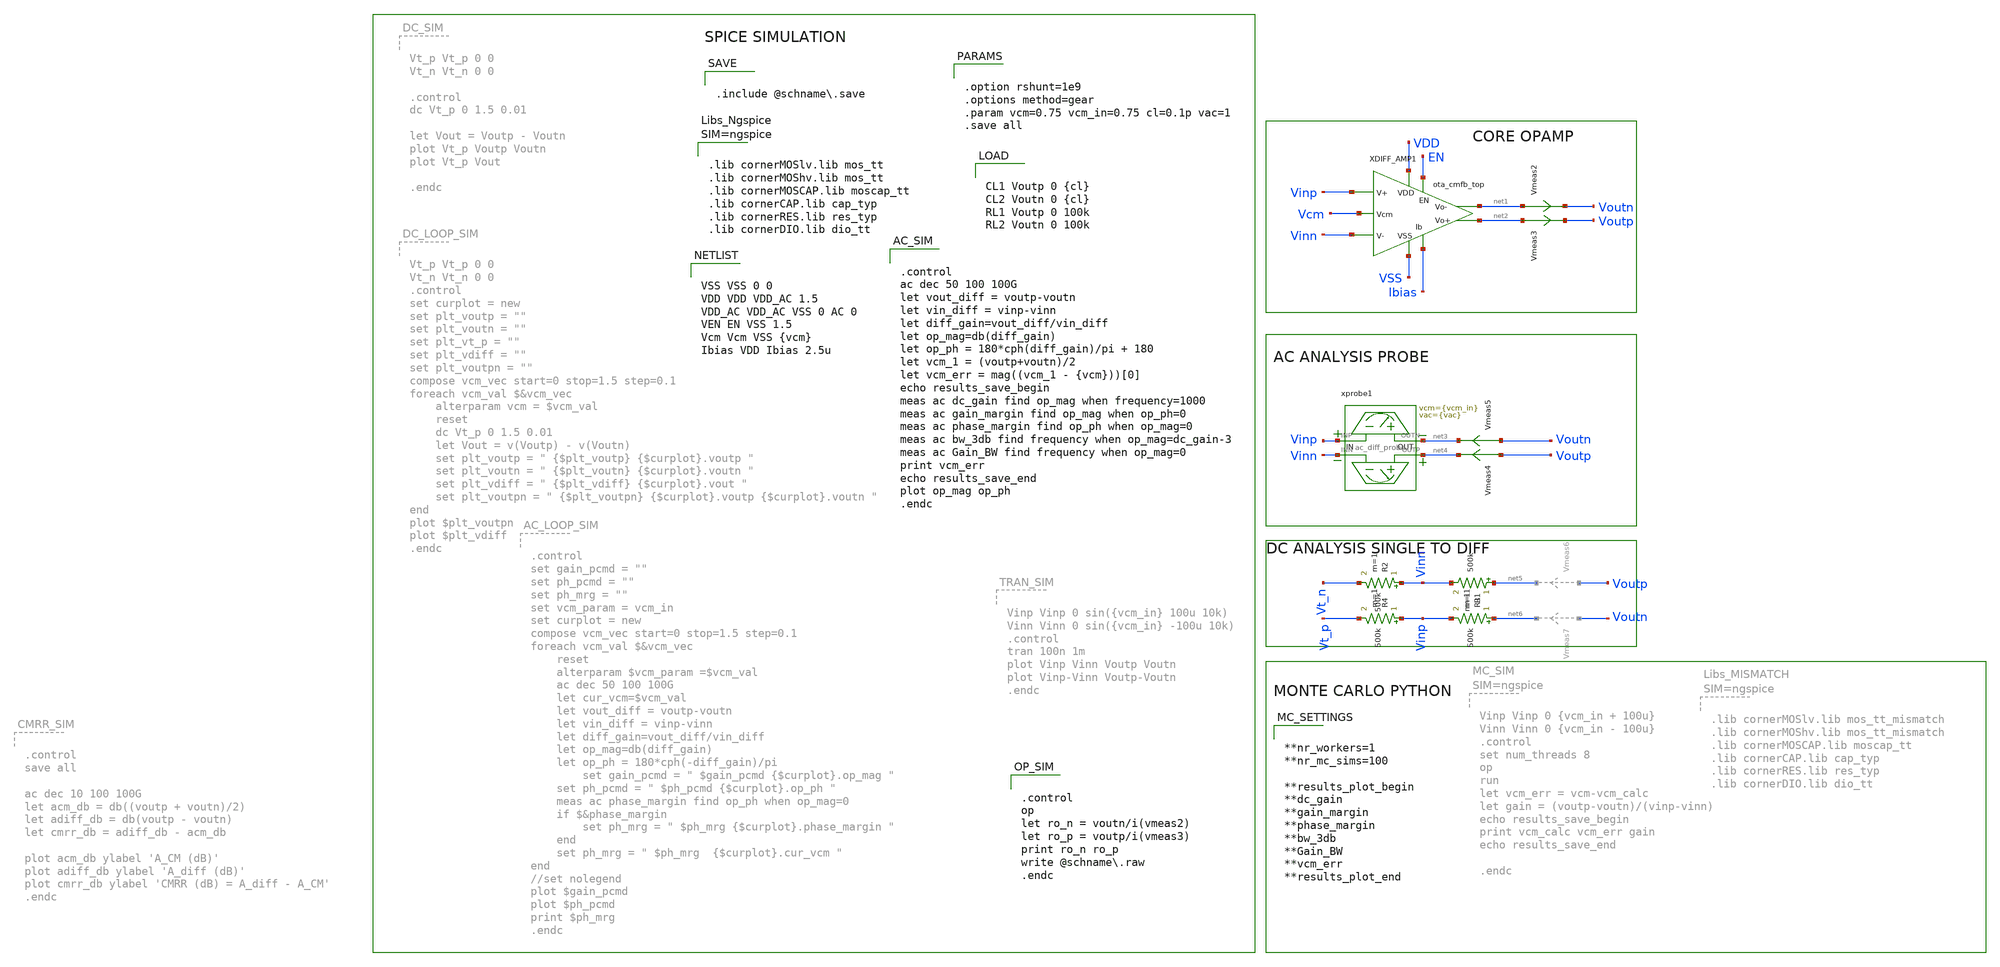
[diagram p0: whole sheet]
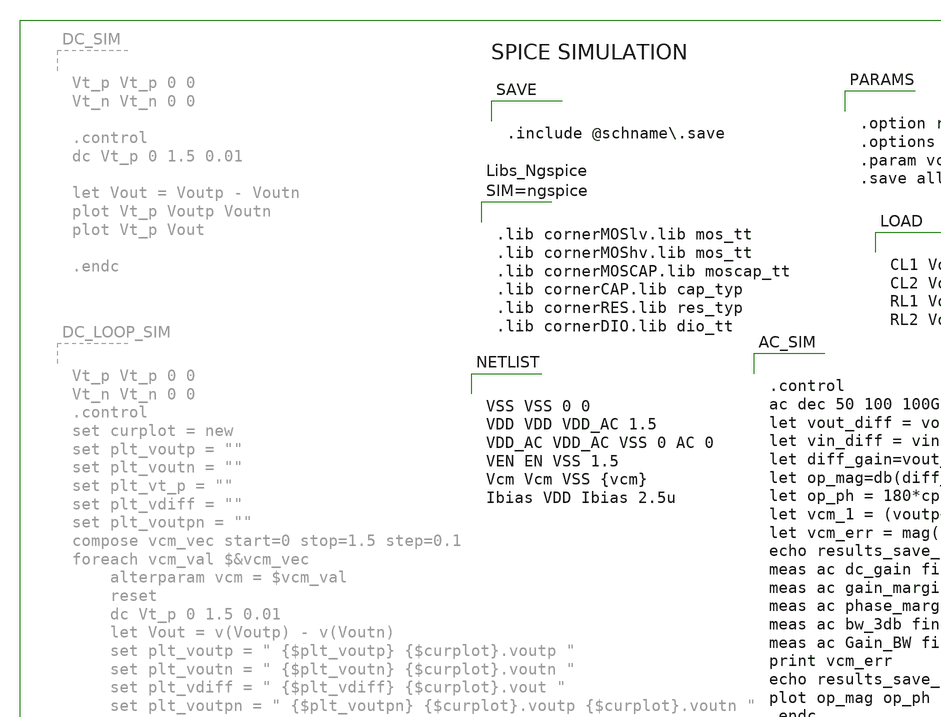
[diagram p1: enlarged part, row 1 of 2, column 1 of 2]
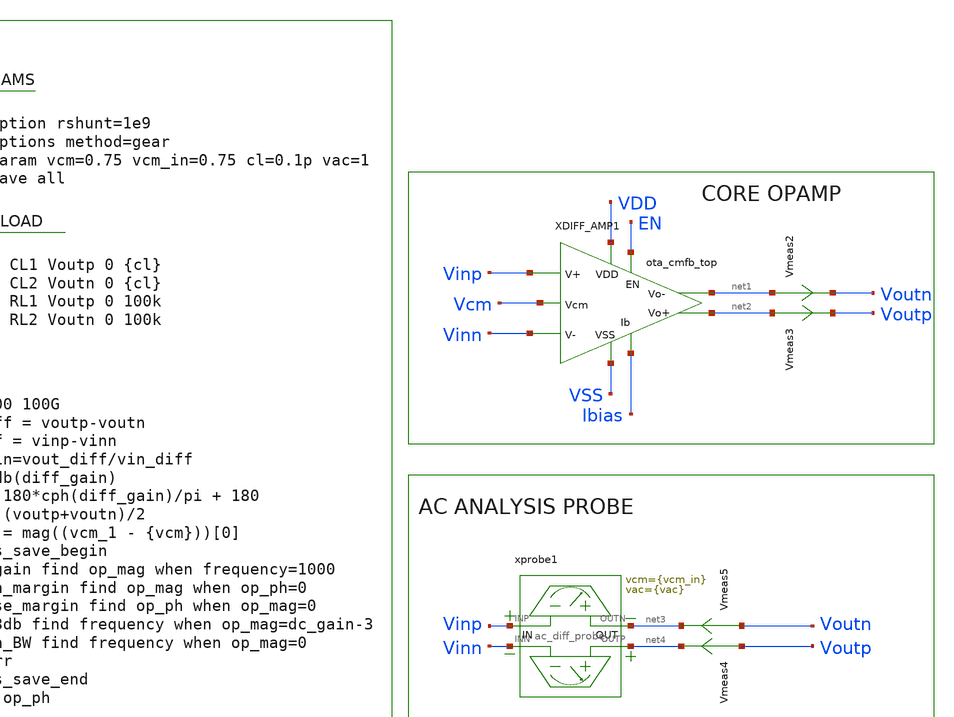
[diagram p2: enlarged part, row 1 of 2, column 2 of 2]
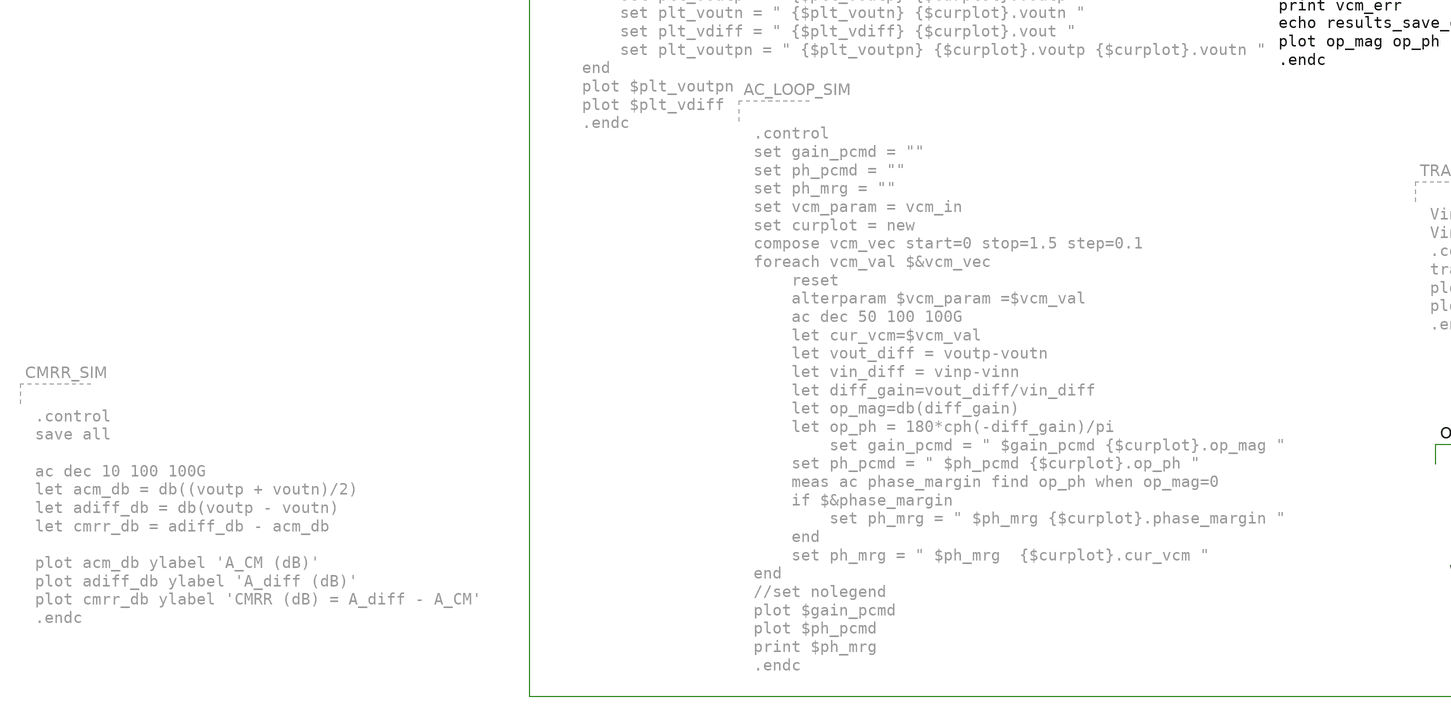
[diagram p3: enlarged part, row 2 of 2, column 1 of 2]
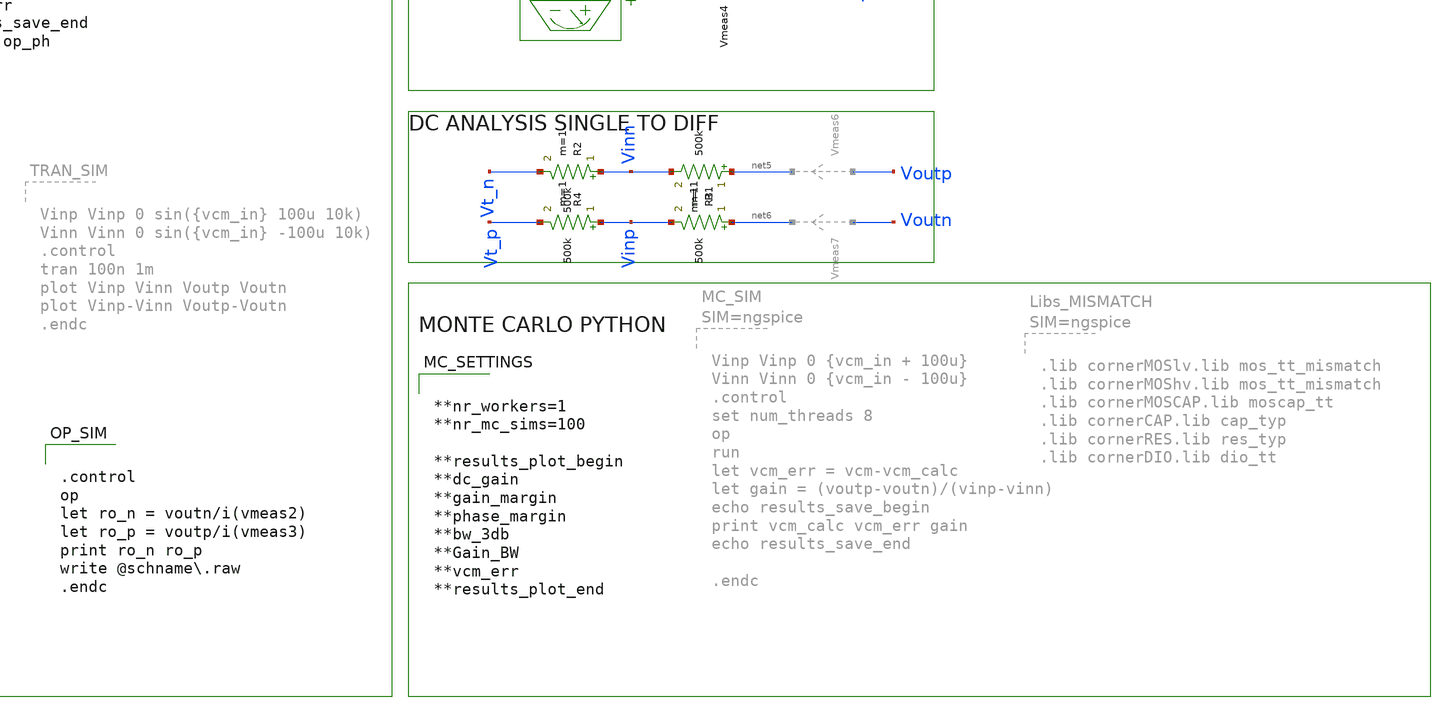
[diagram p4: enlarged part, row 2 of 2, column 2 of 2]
** sch_path: schema/ota_cmfb_top_tb.sch
**.subckt ota_cmfb_top_tb
xprobe1 Vinp net3 Vinn net4 ac_diff_probe vcm={vcm_in} vac={vac}
Vmeas2 net1 Voutn 0
.save i(vmeas2)
Vmeas3 net2 Voutp 0
.save i(vmeas3)
Vmeas4 Voutp net4 0
.save i(vmeas4)
Vmeas5 Voutn net3 0
.save i(vmeas5)
R1 net5 Vinn 500k m=1
R2 Vinn Vt_n 500k m=1
R3 net6 Vinp 500k m=1
R4 Vinp Vt_p 500k m=1
XDIFF_AMP1 Vcm VDD EN Vinp net1 net2 Vinn VSS Ibias ota_cmfb_top
**** begin user architecture code


VSS VSS 0 0
VDD VDD VDD_AC 1.5
VDD_AC VDD_AC VSS 0 AC 0
VEN EN VSS 1.5
Vcm Vcm VSS {vcm}
Ibias VDD Ibias 2.5u



.control
op
let ro_n = voutn/i(vmeas2)
let ro_p = voutp/i(vmeas3)
print ro_n ro_p
write @schname.raw
.endc




.lib cornerMOSlv.lib mos_tt
.lib cornerMOShv.lib mos_tt
.lib cornerMOSCAP.lib moscap_tt
.lib cornerCAP.lib cap_typ
.lib cornerRES.lib res_typ
.lib cornerDIO.lib dio_tt





.control
ac dec 50 100 100G
let vout_diff = voutp-voutn
let vin_diff = vinp-vinn
let diff_gain=vout_diff/vin_diff
let op_mag=db(diff_gain)
let op_ph = 180*cph(diff_gain)/pi + 180
let vcm_1 = (voutp+voutn)/2
let vcm_err = mag((vcm_1 - {vcm}))[0]
echo results_save_begin
meas ac dc_gain find op_mag when frequency=1000
meas ac gain_margin find op_mag when op_ph=0
meas ac phase_margin find op_ph when op_mag=0
meas ac bw_3db find frequency when op_mag=dc_gain-3
meas ac Gain_BW find frequency when op_mag=0
print vcm_err
echo results_save_end
plot op_mag op_ph
.endc




.option rshunt=1e9
.options method=gear
.param vcm=0.75 vcm_in=0.75 cl=0.1p vac=1
.save all




CL1 Voutp 0 {cl}
CL2 Voutn 0 {cl}
RL1 Voutp 0 100k
RL2 Voutn 0 100k



.include @schname.save



**nr_workers=1
**nr_mc_sims=100

**results_plot_begin
**dc_gain
**gain_margin
**phase_margin
**bw_3db
**Gain_BW
**vcm_err
**results_plot_end


**** end user architecture code
**.ends

* expanding   symbol:  ac_diff_probe/ac_diff_probe.sym # of pins=4
** sym_path: schema/ac_diff_probe/ac_diff_probe.sym
** sch_path: schema/ac_diff_probe/ac_diff_probe.sch
.subckt ac_diff_probe INP OUTN INN OUTP  vcm=0.75 vac=0.1
*.iopin OUTN
*.iopin INP
*.iopin OUTP
*.iopin INN
xprobe1 OUTN INP ac_probe vcm={vcm} vac={vac}
xprobe2 OUTP INN ac_probe vcm={vcm} vac=-{vac}
.ends


* expanding   symbol:  schema/ota_cmfb_top.sym # of pins=9
** sym_path: schema/ota_cmfb_top.sym
** sch_path: schema/ota_cmfb_top.sch
.subckt ota_cmfb_top Vcm VDD EN Vinp Voutn Voutp Vinn VSS Ibias
*.iopin VDD
*.ipin Vinn
*.ipin Vinp
*.ipin Ibias
*.opin Voutn
*.opin Voutp
*.iopin VSS
*.ipin EN
*.ipin Vcm
xopamp1 VDD Vcm_reg Vinn Vinp Ibias Voutn Voutp VSS EN Vbias ota_cmfb_core
xota1 VDD EN Vbias Vcm_calc Vcm Vcm_reg VSS ota_cmfb_fbota
XM7 VSS VSS Vbias VSS sg13_lv_nmos w=0.25u l=0.5u ng=1 m=2 mm_ok=1
XR1 Voutn Vcm_calc VSS rhigh w=0.5e-6 l=1e-6*10 m=1 b=0 mm_ok=1
XR2 Voutp Vcm_calc VSS rhigh w=0.5e-6 l=1e-6*10 m=1 b=0 mm_ok=1
XM1 VSS VSS VSS VSS sg13_lv_nmos w=3.2u l=0.5u ng=1 m=10 mm_ok=1
XM2 VDD VDD VDD VDD sg13_lv_pmos w=1.985u l=0.5u ng=1 m=100 mm_ok=1
XD1 VSS EN dantenna l=0.78u w=0.78u
XD2 EN VDD dpantenna l=1.34u w=1.05u
XPCLAMP1 VDD VSS Voutp sg13cmos5l_Clamp_P20N0D
XPCLAMP2 VDD VSS Voutn sg13cmos5l_Clamp_P20N0D
XPCLAMP3 VDD VSS Vcm sg13cmos5l_Clamp_P20N0D
**** begin user architecture code


.include $::SG13CMOS5L_YACINESOT_IP_ROOT/schema/sg13cmos5l_Clamp_P20N0D/sg13cmos5l_Clamp_P20N0D.spice


**** end user architecture code
.ends


* expanding   symbol:  ac_probe/ac_probe.sym # of pins=2
** sym_path: schema/ac_probe/ac_probe.sym
** sch_path: schema/ac_probe/ac_probe.sch
.subckt ac_probe OUT IN  vcm=0.75 vac=0.01

*.iopin IN
*.iopin OUT
C1 0 IN 1 m=1
V1 IN 0 {vcm} ac {vac}
R1 OUT IN 1G m=1
.ends


* expanding   symbol:  ota_cmfb_core/ota_cmfb_core.sym # of pins=10
** sym_path: schema/ota_cmfb_core/ota_cmfb_core.sym
** sch_path: schema/ota_cmfb_core/ota_cmfb_core.sch
.subckt ota_cmfb_core VDD Vcm_reg Vinn Vinp Ibias Voutn Voutp VSS EN Vbias
*.opin Voutn
*.opin Voutp
*.iopin VDD
*.iopin VSS
*.ipin Vinp
*.ipin Ibias
*.ipin Vinn
*.ipin Vcm_reg
*.ipin EN
*.opin Vbias
XMD Voutp_st1 Vbias VSS VSS sg13_lv_nmos w=0.25u l=10u ng=1 m=8 mm_ok=1
XMB src_ab Vinn Voutp_st1 VDD sg13_lv_pmos w=2.5u l=2u ng=1 m=8 mm_ok=1
XMC Voutn_st1 Vbias VSS VSS sg13_lv_nmos w=0.25u l=10u ng=1 m=8 mm_ok=1
XMA src_ab Vinp Voutn_st1 VDD sg13_lv_pmos w=2.5u l=2u ng=1 m=8 mm_ok=1
XMM VDD Vcm_reg src_ab VDD sg13_lv_pmos w=2.5u l=10u ng=1 m=8 mm_ok=1
XME Vbias Vbias VSS VSS sg13_lv_nmos w=0.25u l=10u ng=1 m=2 mm_ok=1
xsf1 VDD Voutn_st1 Voutp Vbias VSS EN ota_cmfb_core_push_pull_output_stage
xsf2 VDD Voutp_st1 Voutn Vbias VSS EN ota_cmfb_core_push_pull_output_stage
XMN0 EN_N EN VSS VSS sg13_lv_nmos w=2.96u l=130.00n ng=1 m=1 mm_ok=1
XMP0 EN_N EN VDD VDD sg13_lv_pmos w=4.48u l=130.00n ng=1 m=1 mm_ok=1
XMN1 Vbias EN_N VSS VSS sg13_lv_nmos w=740.00n l=130.00n ng=1 m=1 mm_ok=1
XMP1 Vcm_reg EN VDD VDD sg13_lv_pmos w=150.00n l=130.00n ng=1 m=1 mm_ok=1
XMB1 VDD VDD src_ab VDD sg13_lv_pmos w=2.5u l=0.5u ng=1 m=4 mm_ok=1
XMN2 Ibias EN Vbias VSS sg13_lv_nmos w=740.00n l=130.00n ng=1 m=1 mm_ok=1
.ends


* expanding   symbol:  ota_cmfb_fbota/ota_cmfb_fbota.sym # of pins=7
** sym_path: schema/ota_cmfb_fbota/ota_cmfb_fbota.sym
** sch_path: schema/ota_cmfb_fbota/ota_cmfb_fbota.sch
.subckt ota_cmfb_fbota VDD EN Ibias Vinn Vinp Vout VSS
*.opin Vout
*.iopin VDD
*.iopin VSS
*.ipin Vinp
*.ipin Ibias
*.ipin Vinn
*.ipin EN
XMJ Vout mirror VSS VSS sg13_lv_nmos w=0.25u l=10u ng=1 m=4 mm_ok=1
XML Vout Vinn src_kl VDD sg13_lv_pmos w=2.5u l=2u ng=1 m=2 mm_ok=1
XMI mirror mirror VSS VSS sg13_lv_nmos w=0.25u l=10u ng=1 m=4 mm_ok=1
XMK mirror Vinp src_kl VDD sg13_lv_pmos w=2.5u l=2u ng=1 m=2 mm_ok=1
XMO src_kl tail_bias VDD VDD sg13_lv_pmos w=1.25u l=5u ng=1 m=8 mm_ok=1
XMN VDD tail_bias tail_bias VDD sg13_lv_pmos w=1.25u l=5u ng=1 m=2 mm_ok=1
XMH tail_bias Ibias VSS VSS sg13_lv_nmos w=0.25u l=10u ng=1 m=2 mm_ok=1
XMN1 mirror EN_N VSS VSS sg13_lv_nmos w=740.00n l=130.00n ng=1 m=1 mm_ok=1
XM2 VSS VSS tail_bias VSS sg13_lv_nmos w=0.25u l=0.5u ng=1 m=2 mm_ok=1
XMK1 mirror VDD VDD VDD sg13_lv_pmos w=2.5u l=0.5u ng=1 m=1 mm_ok=1
XMK2 Vout VDD VDD VDD sg13_lv_pmos w=2.5u l=0.5u ng=1 m=1 mm_ok=1
XMK3 src_kl VDD VDD VDD sg13_lv_pmos w=2.5u l=0.5u ng=1 m=2 mm_ok=1
XMK4 tail_bias VDD VDD VDD sg13_lv_pmos w=1.25u l=0.5u ng=1 m=2 mm_ok=1
XMN0 EN_N EN VSS VSS sg13_lv_nmos w=2.96u l=130.00n ng=1 m=1 mm_ok=1
XMP0 EN_N EN VDD VDD sg13_lv_pmos w=4.48u l=130.00n ng=1 m=1 mm_ok=1
.ends


* expanding   symbol:  ota_cmfb_core/ota_cmfb_core_push_pull_output_stage.sym # of pins=6
** sym_path: schema/ota_cmfb_core/ota_cmfb_core_push_pull_output_stage.sym
** sch_path: schema/ota_cmfb_core/ota_cmfb_core_push_pull_output_stage.sch
.subckt ota_cmfb_core_push_pull_output_stage VDD Vin Vout Vbias VSS EN
*.iopin VSS
*.iopin VDD
*.ipin Vbias
*.ipin Vin
*.opin Vout
*.ipin EN
XM1 Vout Vin_shifted VSS VSS sg13_lv_nmos w=0.5u l=10u ng=1 m=1 mm_ok=1
XM2 VDD Vin Vout VDD sg13_lv_pmos w=5u l=0.5u ng=1 m=1 mm_ok=1
XMC VDD Vbiasp CD_DRN VDD sg13_lv_pmos w=2.5u l=3u ng=1 m=4 mm_ok=1
XME Vin_shifted Vcasp2 Vin VDD sg13_lv_pmos w=2.5u l=3u ng=1 m=2 mm_ok=1
XMD CD_DRN Vcasp Vin VDD sg13_lv_pmos w=2.5u l=3u ng=1 m=4 mm_ok=1
XMN Vin Vcasn2 Vin_shifted VSS sg13_lv_nmos w=0.7u l=3u ng=1 m=2 mm_ok=1
XMH VDD Vbiasp net1 VDD sg13_lv_pmos w=2.5u l=3u ng=1 m=4 mm_ok=1
XMI net1 Vcasp Vcasp VDD sg13_lv_pmos w=2.5u l=3u ng=1 m=4 mm_ok=1
XMJ Vcasp Vcasp2 Vcasp2 VDD sg13_lv_pmos w=2.5u l=3u ng=1 m=4 mm_ok=1
XMB VDD Vbiasp Vcasn2 VDD sg13_lv_pmos w=2.5u l=3u ng=1 m=4 mm_ok=1
XMO Vcasn2 Vcasn2 Vcasn VSS sg13_lv_nmos w=0.7u l=3u ng=1 m=4 mm_ok=1
XR1 net2 Vout VSS rhigh w=0.5e-6 l=1e-6*8 m=1 b=0 mm_ok=1
XC1 Vin net2 sg13_moscap_p w=3.5u l=21.5u m=1 mm_ok=1
XMFG Vbiasp Vbias VSS VSS sg13_lv_nmos w=0.25u l=10u ng=1 m=2 mm_ok=1
XMA VDD Vbiasp Vbiasp VDD sg13_lv_pmos w=2.5u l=3u ng=1 m=10 mm_ok=1
XMP Vcasn Vcasn Vbiasn VSS sg13_lv_nmos w=0.7u l=3u ng=1 m=4 mm_ok=1
XMQ Vbiasn Vbiasn VSS VSS sg13_lv_nmos w=0.7u l=3u ng=1 m=4 mm_ok=1
XMM Vin_shifted Vcasn src_ml VSS sg13_lv_nmos w=0.7u l=3u ng=1 m=4 mm_ok=1
XML src_ml Vbiasn VSS VSS sg13_lv_nmos w=0.7u l=3u ng=1 m=4 mm_ok=1
XMK Vcasp2 Vbiasn VSS VSS sg13_lv_nmos w=0.7u l=3u ng=1 m=4 mm_ok=1
XM3 CD_DRN VDD VDD VDD sg13_lv_pmos w=2.5u l=0.5u ng=1 m=2 mm_ok=1
XM4 Vin_shifted VDD VDD VDD sg13_lv_pmos w=2.5u l=0.5u ng=1 m=1 mm_ok=1
XM5 Vbiasp VDD VDD VDD sg13_lv_pmos w=2.5u l=0.5u ng=1 m=1 mm_ok=1
XM6 Vin VDD VDD VDD sg13_lv_pmos w=2.5u l=0.5u ng=1 m=1 mm_ok=1
XM7 VSS VSS Vin_shifted VSS sg13_lv_nmos w=0.7u l=0.5u ng=1 m=2 mm_ok=1
XM8 VSS VSS Vcasn VSS sg13_lv_nmos w=0.7u l=0.5u ng=1 m=4 mm_ok=1
XMX VSS VSS Vin_shifted VSS sg13_lv_nmos w=0.7u l=3u ng=1 m=4 mm_ok=1
XM9 VSS VSS src_ml VSS sg13_lv_nmos w=0.7u l=0.5u ng=1 m=4 mm_ok=1
XM10 Vcasp VDD VDD VDD sg13_lv_pmos w=2.5u l=0.5u ng=1 m=2 mm_ok=1
XM12 VSS VSS Vbiasp VSS sg13_lv_nmos w=0.25u l=0.5u ng=1 m=2 mm_ok=1
XM13 Vbiasp EN VDD VDD sg13_lv_pmos w=0.15u l=0.13u ng=1 m=1 mm_ok=1
XMN0 EN_N EN VSS VSS sg13_lv_nmos w=2.96u l=130.00n ng=1 m=1 mm_ok=1
XMP0 EN_N EN VDD VDD sg13_lv_pmos w=4.48u l=130.00n ng=1 m=1 mm_ok=1
XMN1 Vbiasn EN_N VSS VSS sg13_lv_nmos w=740.00n l=130.00n ng=1 m=1 mm_ok=1
XM14 Vin EN VDD VDD sg13_lv_pmos w=0.15u l=0.13u ng=1 m=1 mm_ok=1
.ends

.end
